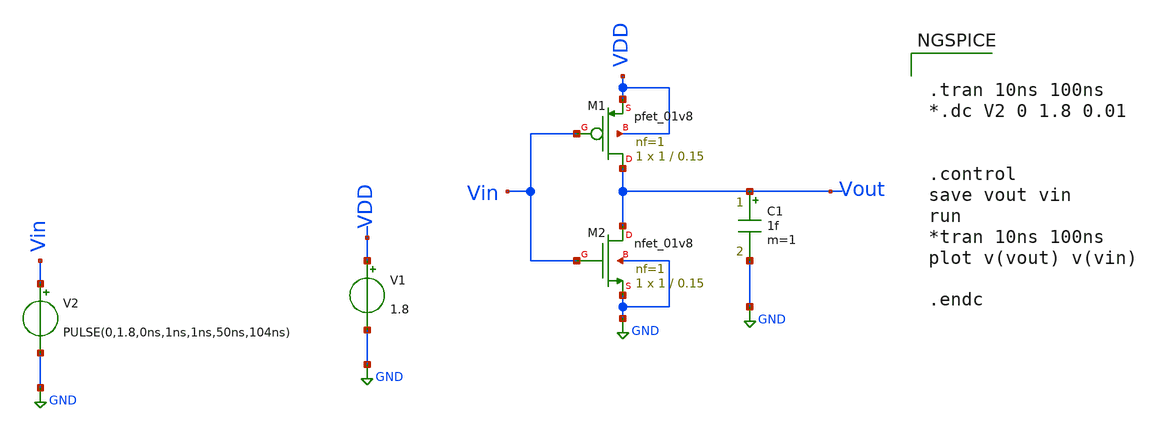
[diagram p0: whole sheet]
** sch_path: eee351_lab.sch
**.subckt eee351_lab
V1 VDD GND 1.8
V2 Vin GND PULSE(0,1.8,0ns,1ns,1ns,50ns,104ns)
C1 Vout GND 1f m=1
XM1 Vout Vin VDD VDD sky130_fd_pr__pfet_01v8 L=0.15 W=1 nf=1 ad='int((nf+1)/2) * W/nf * 0.29' as='int((nf+2)/2) * W/nf * 0.29'
+ pd='2*int((nf+1)/2) * (W/nf + 0.29)' ps='2*int((nf+2)/2) * (W/nf + 0.29)' nrd='0.29 / W' nrs='0.29 / W'
+ sa=0 sb=0 sd=0 mult=1 m=1
XM2 Vout Vin GND GND sky130_fd_pr__nfet_01v8 L=0.15 W=1 nf=1 ad='int((nf+1)/2) * W/nf * 0.29' as='int((nf+2)/2) * W/nf * 0.29'
+ pd='2*int((nf+1)/2) * (W/nf + 0.29)' ps='2*int((nf+2)/2) * (W/nf + 0.29)' nrd='0.29 / W' nrs='0.29 / W'
+ sa=0 sb=0 sd=0 mult=1 m=1
**** begin user architecture code


.tran 10ns 100ns
*.dc V2 0 1.8 0.01


.control
save vout vin
run
*tran 10ns 100ns
plot v(vout) v(vin)

.endc




** opencircuitdesign pdks install
.lib $::SKYWATER_MODELS/sky130.lib.spice tt


**** end user architecture code
**.ends
.GLOBAL GND
.end
